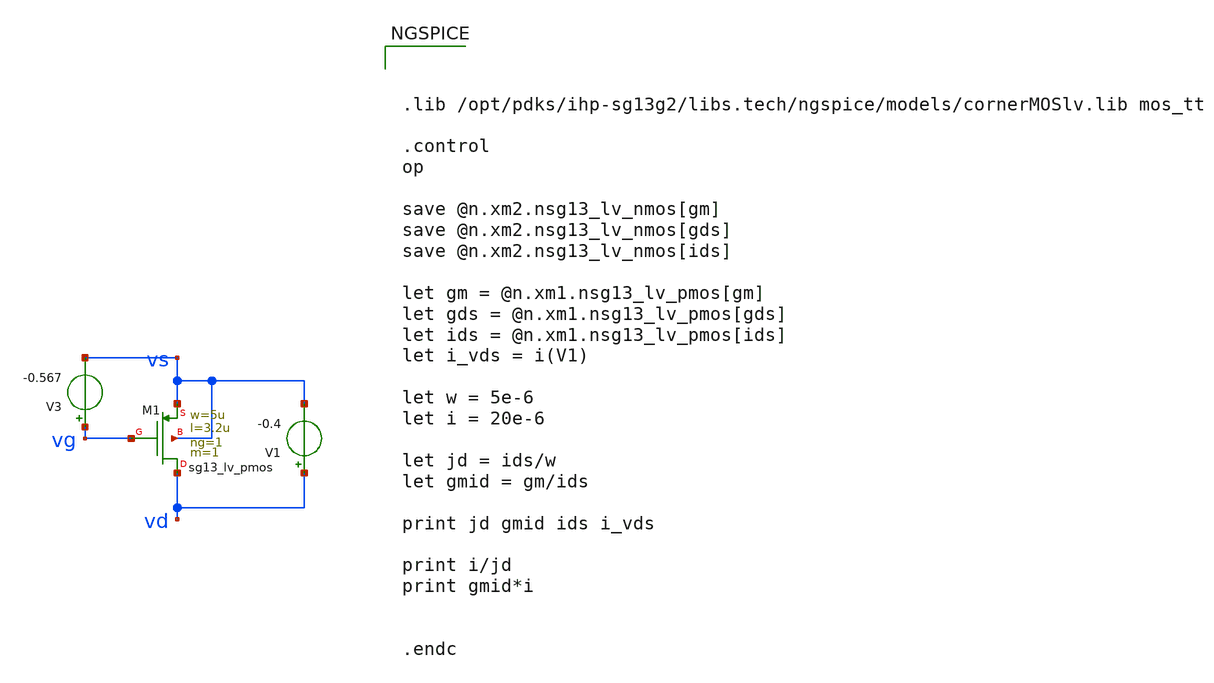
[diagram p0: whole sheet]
** sch_path: test/transitor/xschem/pmos_sweep.sch
**.subckt pmos_sweep
V1 vd vs -0.4
V3 vg vs -0.567
XM1 vd vg vs vs sg13_lv_pmos w=5u l=3.2u ng=1 m=1 mm_ok=1
**** begin user architecture code



.lib /opt/pdks/ihp-sg13g2/libs.tech/ngspice/models/cornerMOSlv.lib mos_tt

.control
op

save @n.xm2.nsg13_lv_nmos[gm]
save @n.xm2.nsg13_lv_nmos[gds]
save @n.xm2.nsg13_lv_nmos[ids]

let gm = @n.xm1.nsg13_lv_pmos[gm]
let gds = @n.xm1.nsg13_lv_pmos[gds]
let ids = @n.xm1.nsg13_lv_pmos[ids]
let i_vds = i(V1)

let w = 5e-6
let i = 20e-6

let jd = ids/w
let gmid = gm/ids

print jd gmid ids i_vds

print i/jd
print gmid*i


.endc



**** end user architecture code
**.ends
.end
